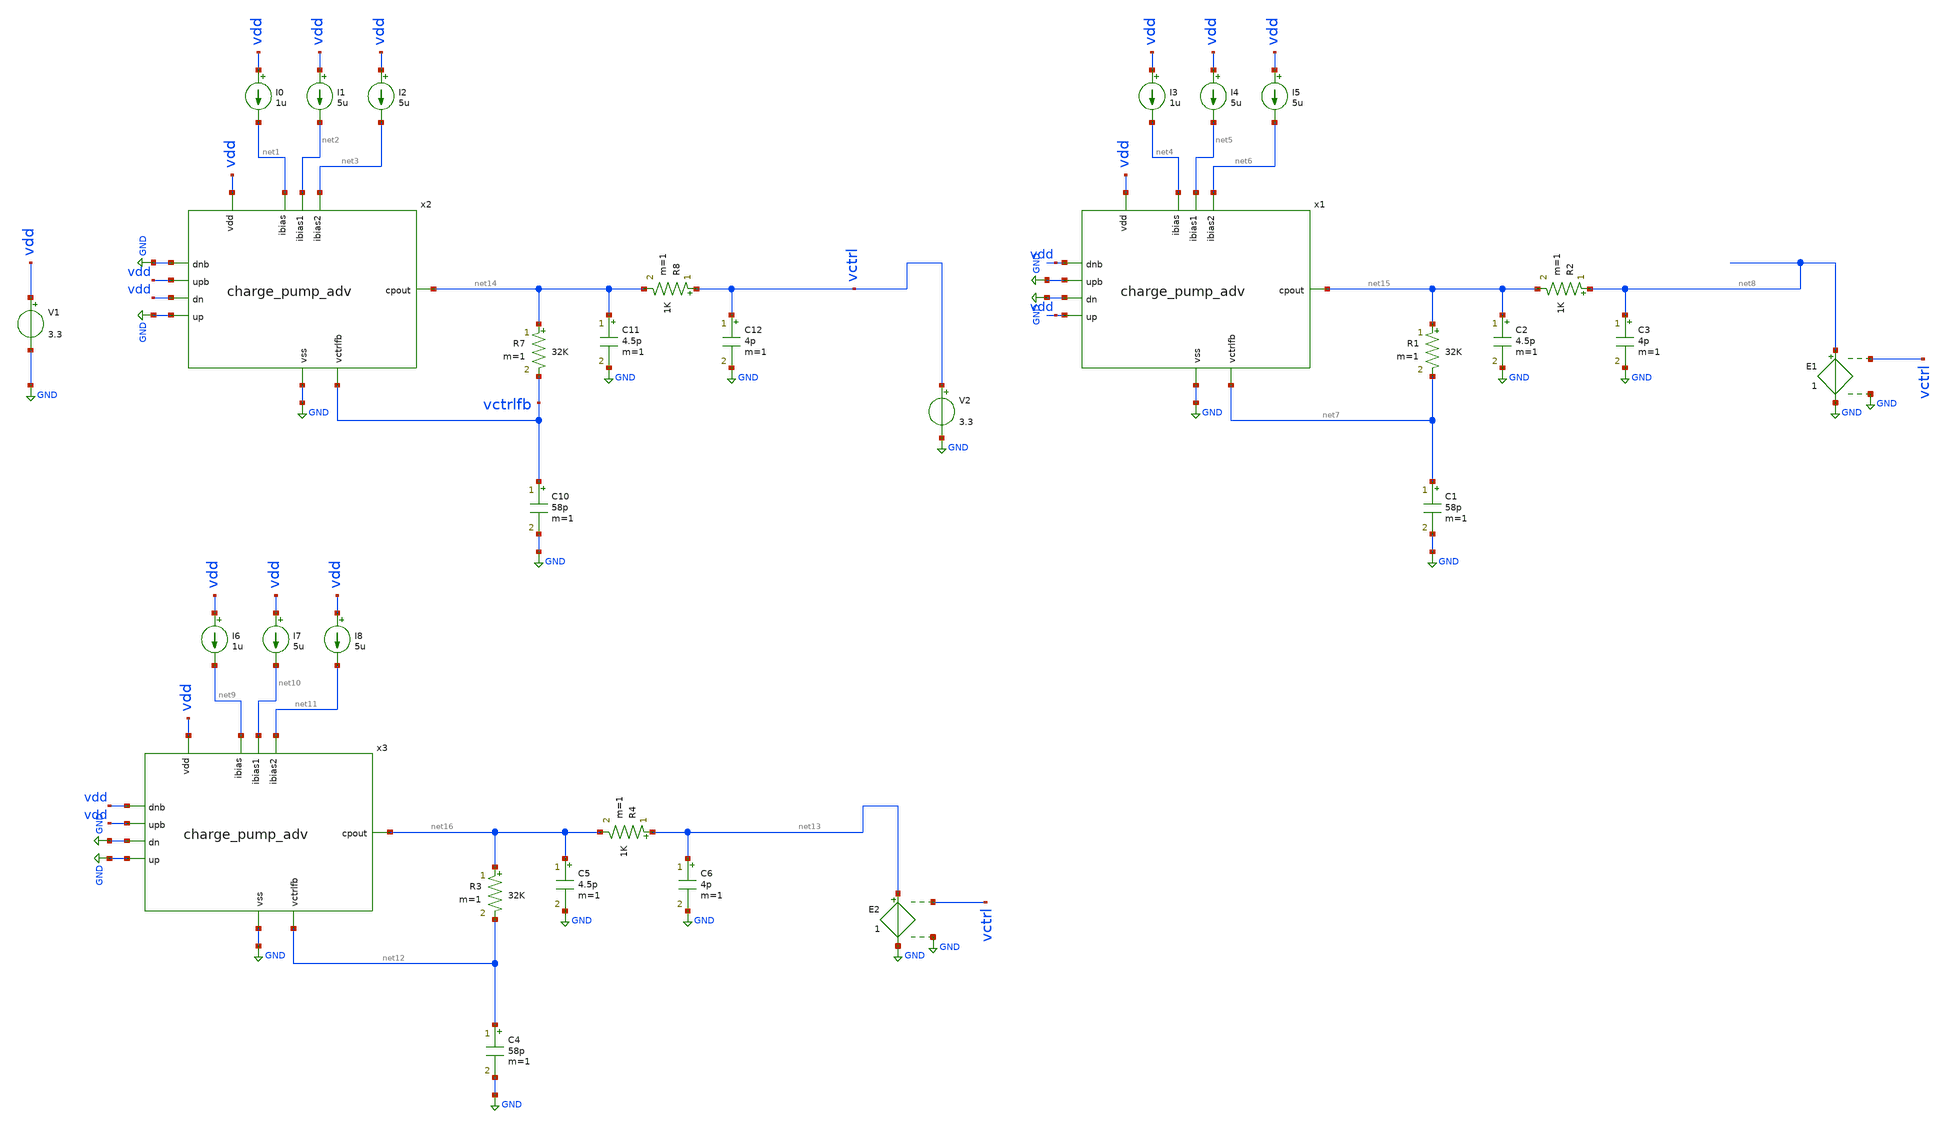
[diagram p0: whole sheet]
** sch_path: xschem/tb_cp_dc.sch
**.subckt tb_cp_dc
I0 vdd net1 1u
I1 vdd net2 5u
I2 vdd net3 5u
x2 vdd GND vdd net2 net3 net14 net1 GND vdd GND vctrlfb charge_pump_adv
V1 vdd GND 3.3
V2 vctrl GND 3.3
I3 vdd net4 1u
I4 vdd net5 5u
I5 vdd net6 5u
x1 vdd vdd GND net5 net6 net15 net4 vdd GND GND net7 charge_pump_adv
E1 net8 GND vctrl GND 1
I6 vdd net9 1u
I7 vdd net10 5u
I8 vdd net11 5u
x3 vdd GND vdd net10 net11 net16 net9 vdd GND GND net12 charge_pump_adv
E2 net13 GND vctrl GND 1
C10 vctrlfb GND 58p m=1
R7 net14 vctrlfb 32K m=1
C11 net14 GND 4.5p m=1
R8 vctrl net14 1K m=1
C12 vctrl GND 4p m=1
C1 net7 GND 58p m=1
R1 net15 net7 32K m=1
C2 net15 GND 4.5p m=1
R2 net8 net15 1K m=1
C3 net8 GND 4p m=1
C4 net12 GND 58p m=1
R3 net16 net12 32K m=1
C5 net16 GND 4.5p m=1
R4 net13 net16 1K m=1
C6 net13 GND 4p m=1
**** begin user architecture code


.include /usr/local/share/pdk/gf180mcuD/libs.tech/ngspice/design.ngspice
.lib /usr/local/share/pdk/gf180mcuD/libs.tech/ngspice/sm141064.ngspice typical
.option temp=25
.control
save all
dc V2 0.1 3.2 0.01
run
plot i(V1)
plot -1*i(V2) i(E1)
plot i(E2) i(E1)+i(V2)


.endc


**** end user architecture code
**.ends

* expanding   symbol:  charge_pump_adv.sym # of pins=11
** sym_path: xschem/charge_pump_adv.sym
** sch_path: xschem/charge_pump_adv.sch
.subckt charge_pump_adv vdd up upb ibias1 ibias2 cpout ibias dnb dn vss vctrlfb
*.ipin vdd
*.ipin vss
*.ipin ibias
*.ipin dn
*.ipin upb
*.ipin up
*.ipin dnb
*.opin cpout
*.ipin ibias1
*.ipin ibias2
*.ipin vctrlfb
XM1 vtailn ibias vss vss nfet_03v3 L=0.5u W=4u nf=1 ad='int((nf+1)/2) * W/nf * 0.18u' as='int((nf+2)/2) * W/nf * 0.18u'
+ pd='2*int((nf+1)/2) * (W/nf + 0.18u)' ps='2*int((nf+2)/2) * (W/nf + 0.18u)' nrd='0.18u / W' nrs='0.18u / W'
+ sa=0 sb=0 sd=0 m=1
XM2 ibias ibias vss vss nfet_03v3 L=0.5u W=4u nf=1 ad='int((nf+1)/2) * W/nf * 0.18u' as='int((nf+2)/2) * W/nf * 0.18u'
+ pd='2*int((nf+1)/2) * (W/nf + 0.18u)' ps='2*int((nf+2)/2) * (W/nf + 0.18u)' nrd='0.18u / W' nrs='0.18u / W'
+ sa=0 sb=0 sd=0 m=1
XM3 cpout dn vtailn vss nfet_03v3 L=0.28u W=12u nf=1 ad='int((nf+1)/2) * W/nf * 0.18u' as='int((nf+2)/2) * W/nf * 0.18u'
+ pd='2*int((nf+1)/2) * (W/nf + 0.18u)' ps='2*int((nf+2)/2) * (W/nf + 0.18u)' nrd='0.18u / W' nrs='0.18u / W'
+ sa=0 sb=0 sd=0 m=1
XM6 vtailp vbiasp vdd vdd pfet_03v3 L=0.5u W=8u nf=1 ad='int((nf+1)/2) * W/nf * 0.18u' as='int((nf+2)/2) * W/nf * 0.18u'
+ pd='2*int((nf+1)/2) * (W/nf + 0.18u)' ps='2*int((nf+2)/2) * (W/nf + 0.18u)' nrd='0.18u / W' nrs='0.18u / W'
+ sa=0 sb=0 sd=0 m=1
XM7 cpout upb vtailp vdd pfet_03v3 L=0.28u W=24u nf=1 ad='int((nf+1)/2) * W/nf * 0.18u' as='int((nf+2)/2) * W/nf * 0.18u'
+ pd='2*int((nf+1)/2) * (W/nf + 0.18u)' ps='2*int((nf+2)/2) * (W/nf + 0.18u)' nrd='0.18u / W' nrs='0.18u / W'
+ sa=0 sb=0 sd=0 m=1
XM8 net1 vbiasp vdd vdd pfet_03v3 L=0.5u W=8u nf=1 ad='int((nf+1)/2) * W/nf * 0.18u' as='int((nf+2)/2) * W/nf * 0.18u'
+ pd='2*int((nf+1)/2) * (W/nf + 0.18u)' ps='2*int((nf+2)/2) * (W/nf + 0.18u)' nrd='0.18u / W' nrs='0.18u / W'
+ sa=0 sb=0 sd=0 m=1
x1 vdd vbiasp ibias1 vrep vctrlfb vss r2r_opamp
XM5 vdummy up vtailp vdd pfet_03v3 L=0.28u W=24u nf=1 ad='int((nf+1)/2) * W/nf * 0.18u' as='int((nf+2)/2) * W/nf * 0.18u'
+ pd='2*int((nf+1)/2) * (W/nf + 0.18u)' ps='2*int((nf+2)/2) * (W/nf + 0.18u)' nrd='0.18u / W' nrs='0.18u / W'
+ sa=0 sb=0 sd=0 m=1
XM9 vdummy dnb vtailn vss nfet_03v3 L=0.28u W=12u nf=1 ad='int((nf+1)/2) * W/nf * 0.18u' as='int((nf+2)/2) * W/nf * 0.18u'
+ pd='2*int((nf+1)/2) * (W/nf + 0.18u)' ps='2*int((nf+2)/2) * (W/nf + 0.18u)' nrd='0.18u / W' nrs='0.18u / W'
+ sa=0 sb=0 sd=0 m=1
x2 vdd vdummy ibias2 cpout vdummy vss r2r_opamp
XM4 vrep vss net1 vdd pfet_03v3 L=0.28u W=24u nf=1 ad='int((nf+1)/2) * W/nf * 0.18u' as='int((nf+2)/2) * W/nf * 0.18u'
+ pd='2*int((nf+1)/2) * (W/nf + 0.18u)' ps='2*int((nf+2)/2) * (W/nf + 0.18u)' nrd='0.18u / W' nrs='0.18u / W'
+ sa=0 sb=0 sd=0 m=1
XM10 vrep vdd net2 vss nfet_03v3 L=0.28u W=12u nf=1 ad='int((nf+1)/2) * W/nf * 0.18u' as='int((nf+2)/2) * W/nf * 0.18u'
+ pd='2*int((nf+1)/2) * (W/nf + 0.18u)' ps='2*int((nf+2)/2) * (W/nf + 0.18u)' nrd='0.18u / W' nrs='0.18u / W'
+ sa=0 sb=0 sd=0 m=1
XM11 net2 ibias vss vss nfet_03v3 L=0.5u W=4u nf=1 ad='int((nf+1)/2) * W/nf * 0.18u' as='int((nf+2)/2) * W/nf * 0.18u'
+ pd='2*int((nf+1)/2) * (W/nf + 0.18u)' ps='2*int((nf+2)/2) * (W/nf + 0.18u)' nrd='0.18u / W' nrs='0.18u / W'
+ sa=0 sb=0 sd=0 m=1
XM12 cpout dnb net3 vss nfet_03v3 L=0.28u W=12u nf=1 ad='int((nf+1)/2) * W/nf * 0.18u' as='int((nf+2)/2) * W/nf * 0.18u'
+ pd='2*int((nf+1)/2) * (W/nf + 0.18u)' ps='2*int((nf+2)/2) * (W/nf + 0.18u)' nrd='0.18u / W' nrs='0.18u / W'
+ sa=0 sb=0 sd=0 m=1
XM13 cpout up net8 vdd pfet_03v3 L=0.28u W=24u nf=1 ad='int((nf+1)/2) * W/nf * 0.18u' as='int((nf+2)/2) * W/nf * 0.18u'
+ pd='2*int((nf+1)/2) * (W/nf + 0.18u)' ps='2*int((nf+2)/2) * (W/nf + 0.18u)' nrd='0.18u / W' nrs='0.18u / W'
+ sa=0 sb=0 sd=0 m=1
C1 net7 vrep 7p m=1
C4 vdummy vss 1p m=1
C3 vdd vbiasp 2p m=1
XM14 vdummy dn net4 vss nfet_03v3 L=0.28u W=12u nf=1 ad='int((nf+1)/2) * W/nf * 0.18u' as='int((nf+2)/2) * W/nf * 0.18u'
+ pd='2*int((nf+1)/2) * (W/nf + 0.18u)' ps='2*int((nf+2)/2) * (W/nf + 0.18u)' nrd='0.18u / W' nrs='0.18u / W'
+ sa=0 sb=0 sd=0 m=1
XM15 vdummy upb net9 vdd pfet_03v3 L=0.28u W=24u nf=1 ad='int((nf+1)/2) * W/nf * 0.18u' as='int((nf+2)/2) * W/nf * 0.18u'
+ pd='2*int((nf+1)/2) * (W/nf + 0.18u)' ps='2*int((nf+2)/2) * (W/nf + 0.18u)' nrd='0.18u / W' nrs='0.18u / W'
+ sa=0 sb=0 sd=0 m=1
* noconn #net3
* noconn #net4
* noconn #net9
* noconn #net8
XM16 net5 ibias vss vss nfet_03v3 L=0.5u W=8u nf=1 ad='int((nf+1)/2) * W/nf * 0.18u' as='int((nf+2)/2) * W/nf * 0.18u'
+ pd='2*int((nf+1)/2) * (W/nf + 0.18u)' ps='2*int((nf+2)/2) * (W/nf + 0.18u)' nrd='0.18u / W' nrs='0.18u / W'
+ sa=0 sb=0 sd=0 m=1
XM17 net6 net6 vdd vdd pfet_03v3 L=0.5u W=16u nf=1 ad='int((nf+1)/2) * W/nf * 0.18u' as='int((nf+2)/2) * W/nf * 0.18u'
+ pd='2*int((nf+1)/2) * (W/nf + 0.18u)' ps='2*int((nf+2)/2) * (W/nf + 0.18u)' nrd='0.18u / W' nrs='0.18u / W'
+ sa=0 sb=0 sd=0 m=1
XM18 net5 net5 net6 vdd pfet_03v3 L=2u W=40u nf=1 ad='int((nf+1)/2) * W/nf * 0.18u' as='int((nf+2)/2) * W/nf * 0.18u'
+ pd='2*int((nf+1)/2) * (W/nf + 0.18u)' ps='2*int((nf+2)/2) * (W/nf + 0.18u)' nrd='0.18u / W' nrs='0.18u / W'
+ sa=0 sb=0 sd=0 m=1
XM19 net7 net5 vbiasp vdd pfet_03v3 L=6u W=40u nf=1 ad='int((nf+1)/2) * W/nf * 0.18u' as='int((nf+2)/2) * W/nf * 0.18u'
+ pd='2*int((nf+1)/2) * (W/nf + 0.18u)' ps='2*int((nf+2)/2) * (W/nf + 0.18u)' nrd='0.18u / W' nrs='0.18u / W'
+ sa=0 sb=0 sd=0 m=1
C2 vrep vss 2p m=1
.ends


* expanding   symbol:  r2r_opamp.sym # of pins=6
** sym_path: xschem/r2r_opamp.sym
** sch_path: xschem/r2r_opamp.sch
.subckt r2r_opamp vdd out ibias inp inm vss
*.ipin vss
*.ipin vdd
*.ipin ibias
*.ipin inp
*.ipin inm
*.opin out
XM1 net3 inp net8 vss nfet_03v3 L=0.28u W=16u nf=1 ad='int((nf+1)/2) * W/nf * 0.18u' as='int((nf+2)/2) * W/nf * 0.18u'
+ pd='2*int((nf+1)/2) * (W/nf + 0.18u)' ps='2*int((nf+2)/2) * (W/nf + 0.18u)' nrd='0.18u / W' nrs='0.18u / W'
+ sa=0 sb=0 sd=0 m=1
XM2 net4 inm net8 vss nfet_03v3 L=0.28u W=16u nf=1 ad='int((nf+1)/2) * W/nf * 0.18u' as='int((nf+2)/2) * W/nf * 0.18u'
+ pd='2*int((nf+1)/2) * (W/nf + 0.18u)' ps='2*int((nf+2)/2) * (W/nf + 0.18u)' nrd='0.18u / W' nrs='0.18u / W'
+ sa=0 sb=0 sd=0 m=1
XM3 net8 ibias vss vss nfet_03v3 L=0.5u W=16u nf=1 ad='int((nf+1)/2) * W/nf * 0.18u' as='int((nf+2)/2) * W/nf * 0.18u'
+ pd='2*int((nf+1)/2) * (W/nf + 0.18u)' ps='2*int((nf+2)/2) * (W/nf + 0.18u)' nrd='0.18u / W' nrs='0.18u / W'
+ sa=0 sb=0 sd=0 m=1
XM4 net6 inp net1 vdd pfet_03v3 L=0.28u W=32u nf=1 ad='int((nf+1)/2) * W/nf * 0.18u' as='int((nf+2)/2) * W/nf * 0.18u'
+ pd='2*int((nf+1)/2) * (W/nf + 0.18u)' ps='2*int((nf+2)/2) * (W/nf + 0.18u)' nrd='0.18u / W' nrs='0.18u / W'
+ sa=0 sb=0 sd=0 m=1
XM5 net7 inm net1 vdd pfet_03v3 L=0.28u W=32u nf=1 ad='int((nf+1)/2) * W/nf * 0.18u' as='int((nf+2)/2) * W/nf * 0.18u'
+ pd='2*int((nf+1)/2) * (W/nf + 0.18u)' ps='2*int((nf+2)/2) * (W/nf + 0.18u)' nrd='0.18u / W' nrs='0.18u / W'
+ sa=0 sb=0 sd=0 m=1
XM6 net1 net2 vdd vdd pfet_03v3 L=0.5u W=32u nf=1 ad='int((nf+1)/2) * W/nf * 0.18u' as='int((nf+2)/2) * W/nf * 0.18u'
+ pd='2*int((nf+1)/2) * (W/nf + 0.18u)' ps='2*int((nf+2)/2) * (W/nf + 0.18u)' nrd='0.18u / W' nrs='0.18u / W'
+ sa=0 sb=0 sd=0 m=1
XM7 net5 vbiasn net6 vss nfet_03v3 L=0.5u W=8u nf=1 ad='int((nf+1)/2) * W/nf * 0.18u' as='int((nf+2)/2) * W/nf * 0.18u'
+ pd='2*int((nf+1)/2) * (W/nf + 0.18u)' ps='2*int((nf+2)/2) * (W/nf + 0.18u)' nrd='0.18u / W' nrs='0.18u / W'
+ sa=0 sb=0 sd=0 m=1
XM8 out vbiasn net7 vss nfet_03v3 L=0.5u W=8u nf=1 ad='int((nf+1)/2) * W/nf * 0.18u' as='int((nf+2)/2) * W/nf * 0.18u'
+ pd='2*int((nf+1)/2) * (W/nf + 0.18u)' ps='2*int((nf+2)/2) * (W/nf + 0.18u)' nrd='0.18u / W' nrs='0.18u / W'
+ sa=0 sb=0 sd=0 m=1
XM9 net6 ibias vss vss nfet_03v3 L=0.5u W=16u nf=1 ad='int((nf+1)/2) * W/nf * 0.18u' as='int((nf+2)/2) * W/nf * 0.18u'
+ pd='2*int((nf+1)/2) * (W/nf + 0.18u)' ps='2*int((nf+2)/2) * (W/nf + 0.18u)' nrd='0.18u / W' nrs='0.18u / W'
+ sa=0 sb=0 sd=0 m=1
XM10 net7 ibias vss vss nfet_03v3 L=0.5u W=16u nf=1 ad='int((nf+1)/2) * W/nf * 0.18u' as='int((nf+2)/2) * W/nf * 0.18u'
+ pd='2*int((nf+1)/2) * (W/nf + 0.18u)' ps='2*int((nf+2)/2) * (W/nf + 0.18u)' nrd='0.18u / W' nrs='0.18u / W'
+ sa=0 sb=0 sd=0 m=1
XM11 net5 vbiasp net3 vdd pfet_03v3 L=0.5u W=16u nf=1 ad='int((nf+1)/2) * W/nf * 0.18u' as='int((nf+2)/2) * W/nf * 0.18u'
+ pd='2*int((nf+1)/2) * (W/nf + 0.18u)' ps='2*int((nf+2)/2) * (W/nf + 0.18u)' nrd='0.18u / W' nrs='0.18u / W'
+ sa=0 sb=0 sd=0 m=1
XM12 out vbiasp net4 vdd pfet_03v3 L=0.5u W=16u nf=1 ad='int((nf+1)/2) * W/nf * 0.18u' as='int((nf+2)/2) * W/nf * 0.18u'
+ pd='2*int((nf+1)/2) * (W/nf + 0.18u)' ps='2*int((nf+2)/2) * (W/nf + 0.18u)' nrd='0.18u / W' nrs='0.18u / W'
+ sa=0 sb=0 sd=0 m=1
XM13 net3 net5 vdd vdd pfet_03v3 L=0.5u W=32u nf=1 ad='int((nf+1)/2) * W/nf * 0.18u' as='int((nf+2)/2) * W/nf * 0.18u'
+ pd='2*int((nf+1)/2) * (W/nf + 0.18u)' ps='2*int((nf+2)/2) * (W/nf + 0.18u)' nrd='0.18u / W' nrs='0.18u / W'
+ sa=0 sb=0 sd=0 m=1
XM14 net4 net5 vdd vdd pfet_03v3 L=0.5u W=32u nf=1 ad='int((nf+1)/2) * W/nf * 0.18u' as='int((nf+2)/2) * W/nf * 0.18u'
+ pd='2*int((nf+1)/2) * (W/nf + 0.18u)' ps='2*int((nf+2)/2) * (W/nf + 0.18u)' nrd='0.18u / W' nrs='0.18u / W'
+ sa=0 sb=0 sd=0 m=1
XM15 ibias ibias vss vss nfet_03v3 L=0.5u W=2u nf=1 ad='int((nf+1)/2) * W/nf * 0.18u' as='int((nf+2)/2) * W/nf * 0.18u'
+ pd='2*int((nf+1)/2) * (W/nf + 0.18u)' ps='2*int((nf+2)/2) * (W/nf + 0.18u)' nrd='0.18u / W' nrs='0.18u / W'
+ sa=0 sb=0 sd=0 m=1
XM16 net2 ibias vss vss nfet_03v3 L=0.5u W=2u nf=1 ad='int((nf+1)/2) * W/nf * 0.18u' as='int((nf+2)/2) * W/nf * 0.18u'
+ pd='2*int((nf+1)/2) * (W/nf + 0.18u)' ps='2*int((nf+2)/2) * (W/nf + 0.18u)' nrd='0.18u / W' nrs='0.18u / W'
+ sa=0 sb=0 sd=0 m=1
XM17 net2 net2 vdd vdd pfet_03v3 L=0.5u W=4u nf=1 ad='int((nf+1)/2) * W/nf * 0.18u' as='int((nf+2)/2) * W/nf * 0.18u'
+ pd='2*int((nf+1)/2) * (W/nf + 0.18u)' ps='2*int((nf+2)/2) * (W/nf + 0.18u)' nrd='0.18u / W' nrs='0.18u / W'
+ sa=0 sb=0 sd=0 m=1
XM18 vbiasp ibias vss vss nfet_03v3 L=0.5u W=8u nf=1 ad='int((nf+1)/2) * W/nf * 0.18u' as='int((nf+2)/2) * W/nf * 0.18u'
+ pd='2*int((nf+1)/2) * (W/nf + 0.18u)' ps='2*int((nf+2)/2) * (W/nf + 0.18u)' nrd='0.18u / W' nrs='0.18u / W'
+ sa=0 sb=0 sd=0 m=1
XM19 vbiasp vbiasp vdd vdd pfet_03v3 L=0.5u W=4u nf=1 ad='int((nf+1)/2) * W/nf * 0.18u' as='int((nf+2)/2) * W/nf * 0.18u'
+ pd='2*int((nf+1)/2) * (W/nf + 0.18u)' ps='2*int((nf+2)/2) * (W/nf + 0.18u)' nrd='0.18u / W' nrs='0.18u / W'
+ sa=0 sb=0 sd=0 m=1
XM20 vbiasn net2 vdd vdd pfet_03v3 L=0.5u W=16u nf=1 ad='int((nf+1)/2) * W/nf * 0.18u' as='int((nf+2)/2) * W/nf * 0.18u'
+ pd='2*int((nf+1)/2) * (W/nf + 0.18u)' ps='2*int((nf+2)/2) * (W/nf + 0.18u)' nrd='0.18u / W' nrs='0.18u / W'
+ sa=0 sb=0 sd=0 m=1
XM21 vbiasn vbiasn vss vss nfet_03v3 L=0.5u W=2u nf=1 ad='int((nf+1)/2) * W/nf * 0.18u' as='int((nf+2)/2) * W/nf * 0.18u'
+ pd='2*int((nf+1)/2) * (W/nf + 0.18u)' ps='2*int((nf+2)/2) * (W/nf + 0.18u)' nrd='0.18u / W' nrs='0.18u / W'
+ sa=0 sb=0 sd=0 m=1
.ends

.GLOBAL GND
.end
